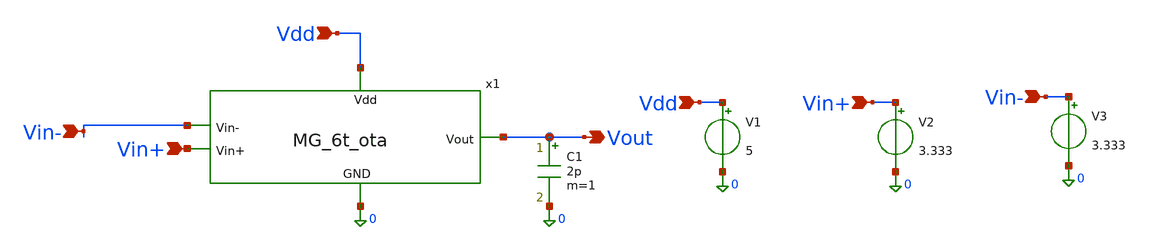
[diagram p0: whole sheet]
** sch_path: MG_6T_OTA/MG_6t_ota_testbench.sch
**.subckt MG_6t_ota_testbench Vdd Vin+ Vin- Vdd Vin+ Vin- Vout
*.ipin Vdd
*.ipin Vin+
*.ipin Vin-
*.ipin Vdd
*.ipin Vin+
*.ipin Vin-
*.opin Vout
V1 Vdd 0 5
V2 Vin+ 0 3.333
V3 Vin- 0 3.333
C1 Vout 0 2p m=1
x1 Vdd Vout Vin- Vin+ 0 MG_6t_ota
**** begin user architecture code



.include /foss/pdks/gf180mcuD/libs.tech/ngspice/design.ngspice
.lib /foss/pdks/gf180mcuD/libs.tech/ngspice/sm141064.ngspice typical
.lib /foss/pdks/gf180mcuD/libs.tech/ngspice/sm141064.ngspice res_typical
.lib /foss/pdks/gf180mcuD/libs.tech/ngspice/sm141064.ngspice moscap_typical
.lib /foss/pdks/gf180mcuD/libs.tech/ngspice/sm141064.ngspice diode_typical

*.control
*  save all
*  op
*  alter v2 ac = 1
*  ac dec 20 1 1G
*  setplot ac1
*
*  let gain_db = vdb(vout)
*  let phase_deg = (180/PI) * ph(vout)
*
*  meas ac dc_gain MAX gain_db
*  meas ac ugbw WHEN gain_db=0 FALL=1
*  meas ac ph_at_ugbw FIND phase_deg WHEN gain_db=0
*  let phase_margin = 180 + ph_at_ugbw
*
*  print dc_gain ugbw phase_margin
*
*  plot gain_db title 'Magnitude Response (dB)'
*  plot phase_deg title 'Phase Response (Degrees)'
*.endc

.control
  let mc_runs = 50
  let run_idx = 1

  * Header for text file
  echo Run_Number DC_Gain_dB UGBW_Hz Phase_Margin_Deg > mc_results.txt

  while run_idx <= mc_runs
    reset

    * THIS IS THE FIX: alter must be applied AFTER reset!
    alter v2 ac = 1

    ac dec 20 1 1G

    let gain_db = vdb(Vout)
    let phase_deg = (180/PI) * ph(Vout)

    meas ac dc_gain MAX gain_db
    meas ac ugbw WHEN gain_db=0 FALL=1
    meas ac ph_at_ugbw FIND phase_deg WHEN gain_db=0
    let phase_margin = 180 + ph_at_ugbw

    * Save data without quotes
    echo $&run_idx $&dc_gain $&ugbw $&phase_margin >> mc_results.txt

    destroy all
    let run_idx = run_idx + 1
  end

  echo Monte Carlo simulation complete check mc_results.txt
.endc



**** end user architecture code
**.ends
.end
